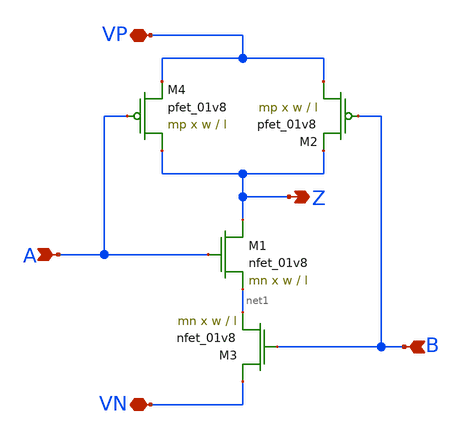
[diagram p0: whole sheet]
** sch_path: schematics/nand.sch
**.subckt nand A VP VN Z B
*.ipin A
*.iopin VP
*.iopin VN
*.opin Z
*.ipin B
XM1 Z A net1 GND sky130_fd_pr__nfet_01v8 L=l W=w nf=1 ad='int((nf+1)/2) * W/nf * 0.29' as='int((nf+2)/2) * W/nf * 0.29'
+ pd='2*int((nf+1)/2) * (W/nf + 0.29)' ps='2*int((nf+2)/2) * (W/nf + 0.29)' nrd='0.29 / W' nrs='0.29 / W'
+ sa=0 sb=0 sd=0 mult=mn m=mn
XM2 VP B Z VDD sky130_fd_pr__pfet_01v8 L=l W=w nf=1 ad='int((nf+1)/2) * W/nf * 0.29' as='int((nf+2)/2) * W/nf * 0.29'
+ pd='2*int((nf+1)/2) * (W/nf + 0.29)' ps='2*int((nf+2)/2) * (W/nf + 0.29)' nrd='0.29 / W' nrs='0.29 / W'
+ sa=0 sb=0 sd=0 mult=mp m=mp
XM3 VN B net1 GND sky130_fd_pr__nfet_01v8 L=l W=w nf=1 ad='int((nf+1)/2) * W/nf * 0.29' as='int((nf+2)/2) * W/nf * 0.29'
+ pd='2*int((nf+1)/2) * (W/nf + 0.29)' ps='2*int((nf+2)/2) * (W/nf + 0.29)' nrd='0.29 / W' nrs='0.29 / W'
+ sa=0 sb=0 sd=0 mult=mn m=mn
XM4 Z A VP VDD sky130_fd_pr__pfet_01v8 L=l W=w nf=1 ad='int((nf+1)/2) * W/nf * 0.29' as='int((nf+2)/2) * W/nf * 0.29'
+ pd='2*int((nf+1)/2) * (W/nf + 0.29)' ps='2*int((nf+2)/2) * (W/nf + 0.29)' nrd='0.29 / W' nrs='0.29 / W'
+ sa=0 sb=0 sd=0 mult=mp m=mp
**.ends
.end
